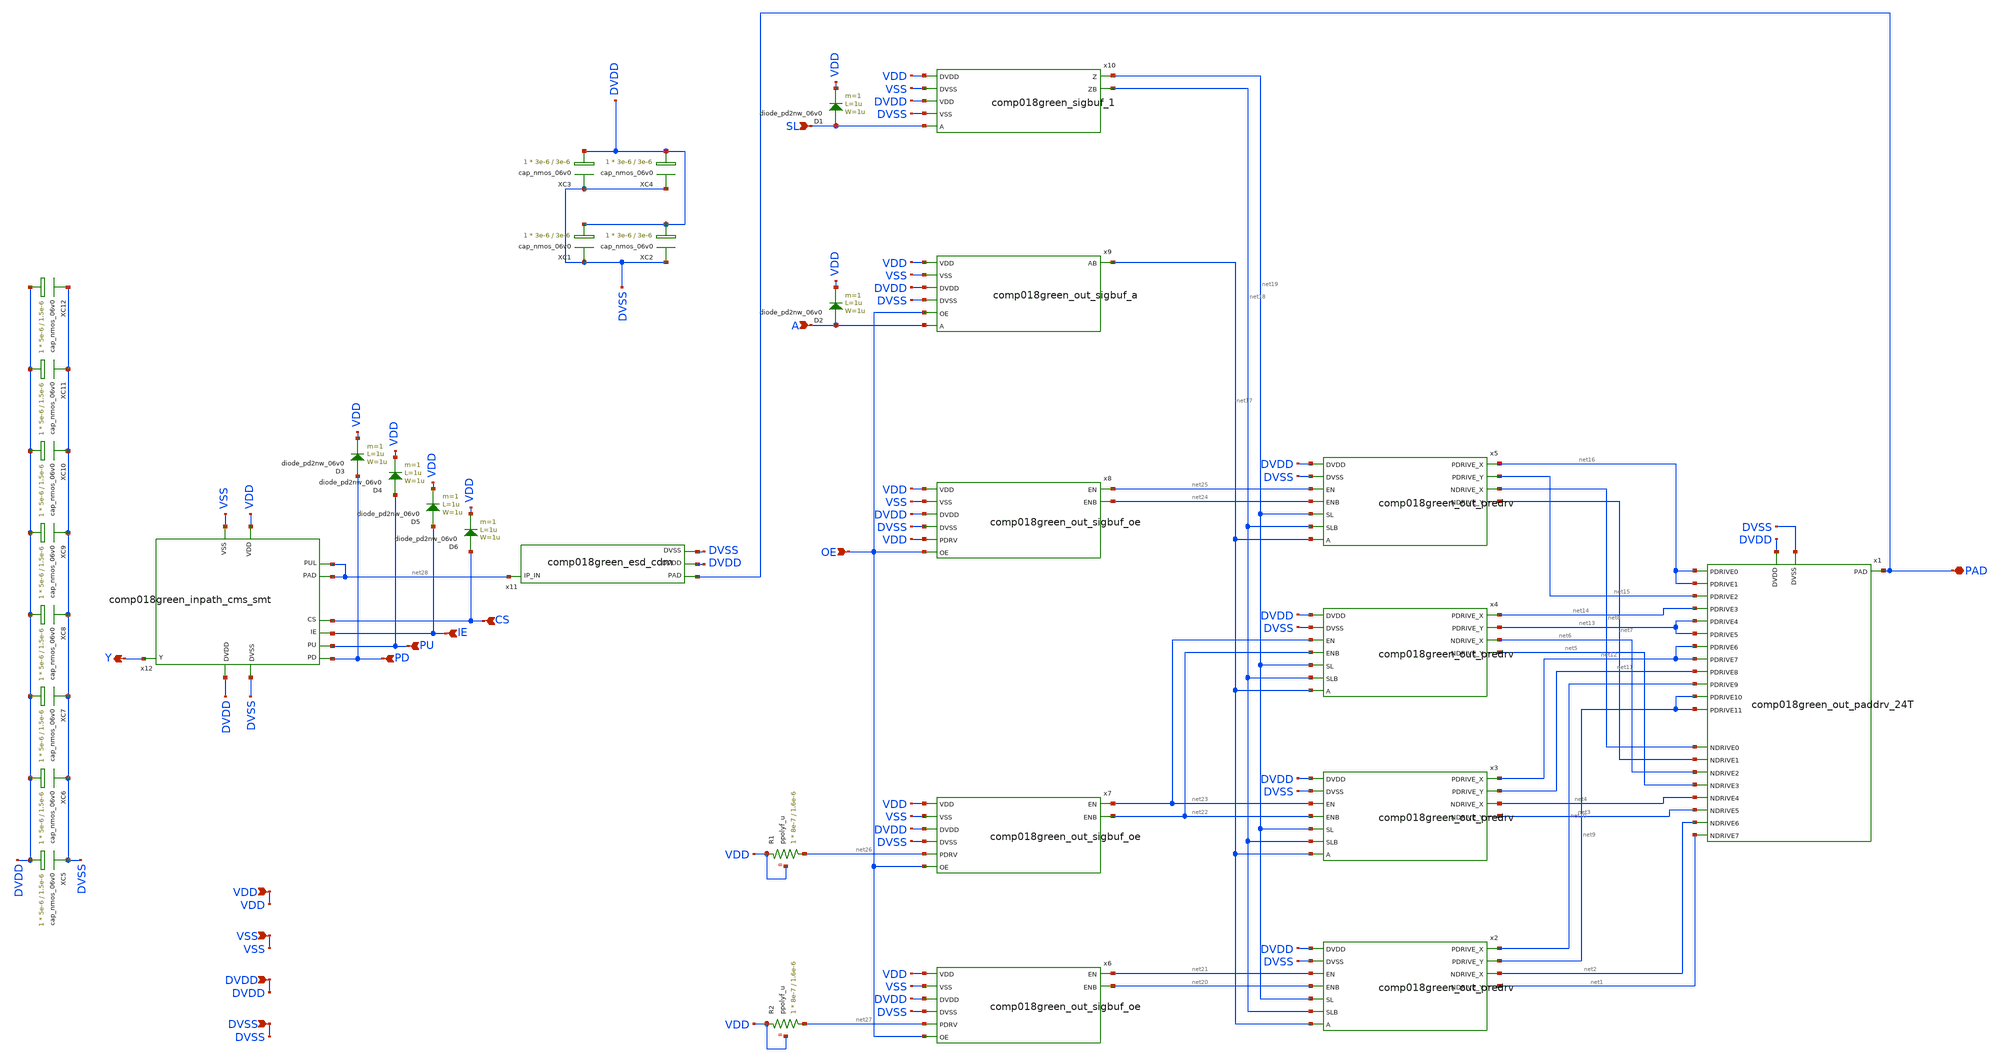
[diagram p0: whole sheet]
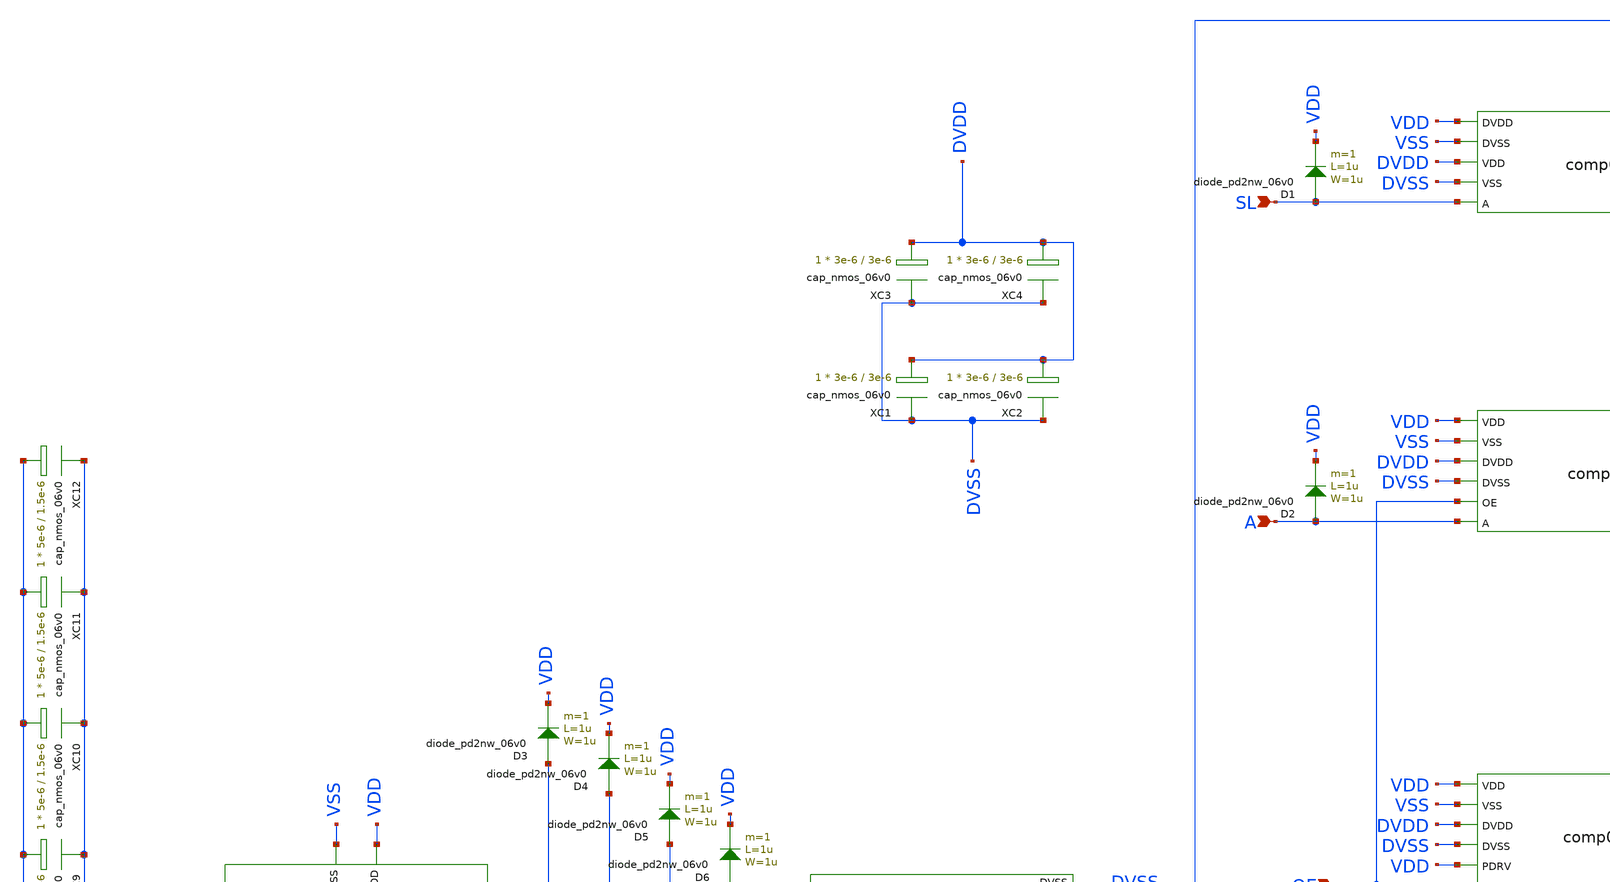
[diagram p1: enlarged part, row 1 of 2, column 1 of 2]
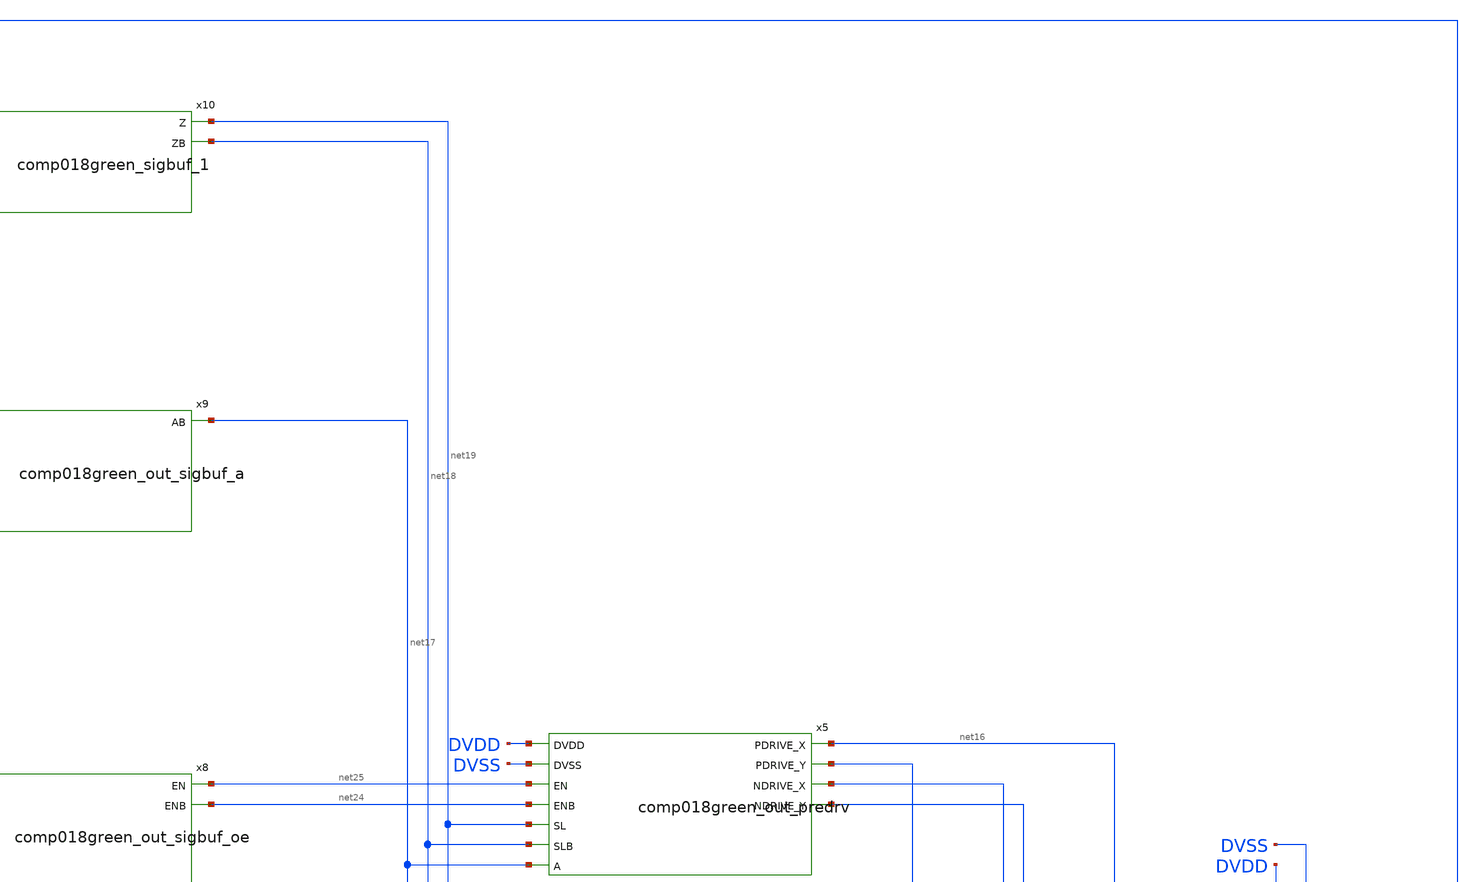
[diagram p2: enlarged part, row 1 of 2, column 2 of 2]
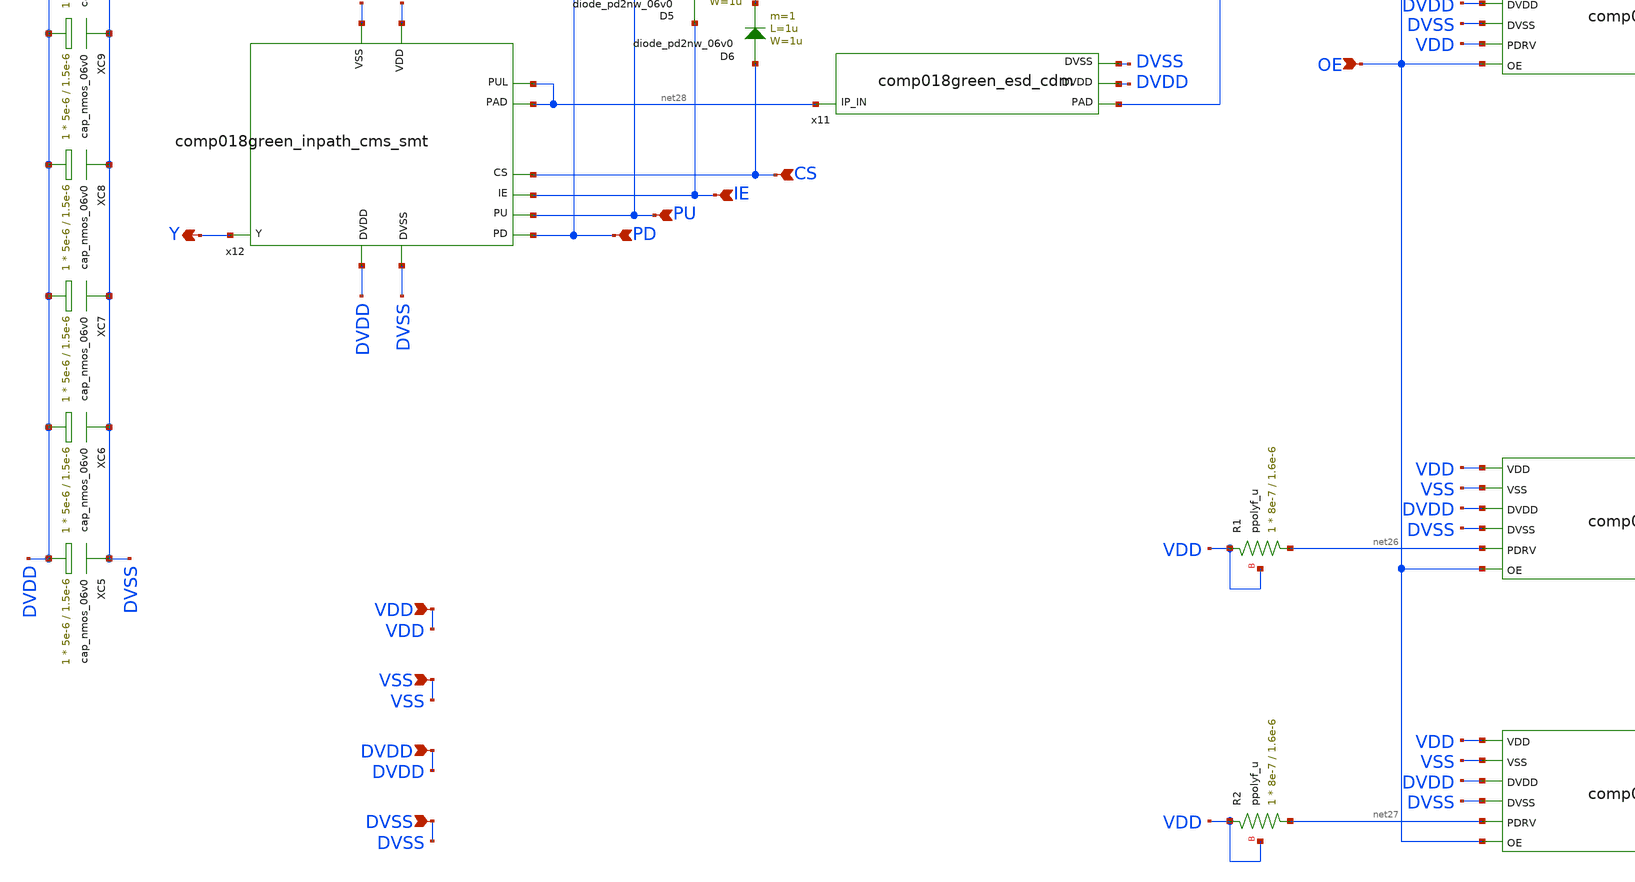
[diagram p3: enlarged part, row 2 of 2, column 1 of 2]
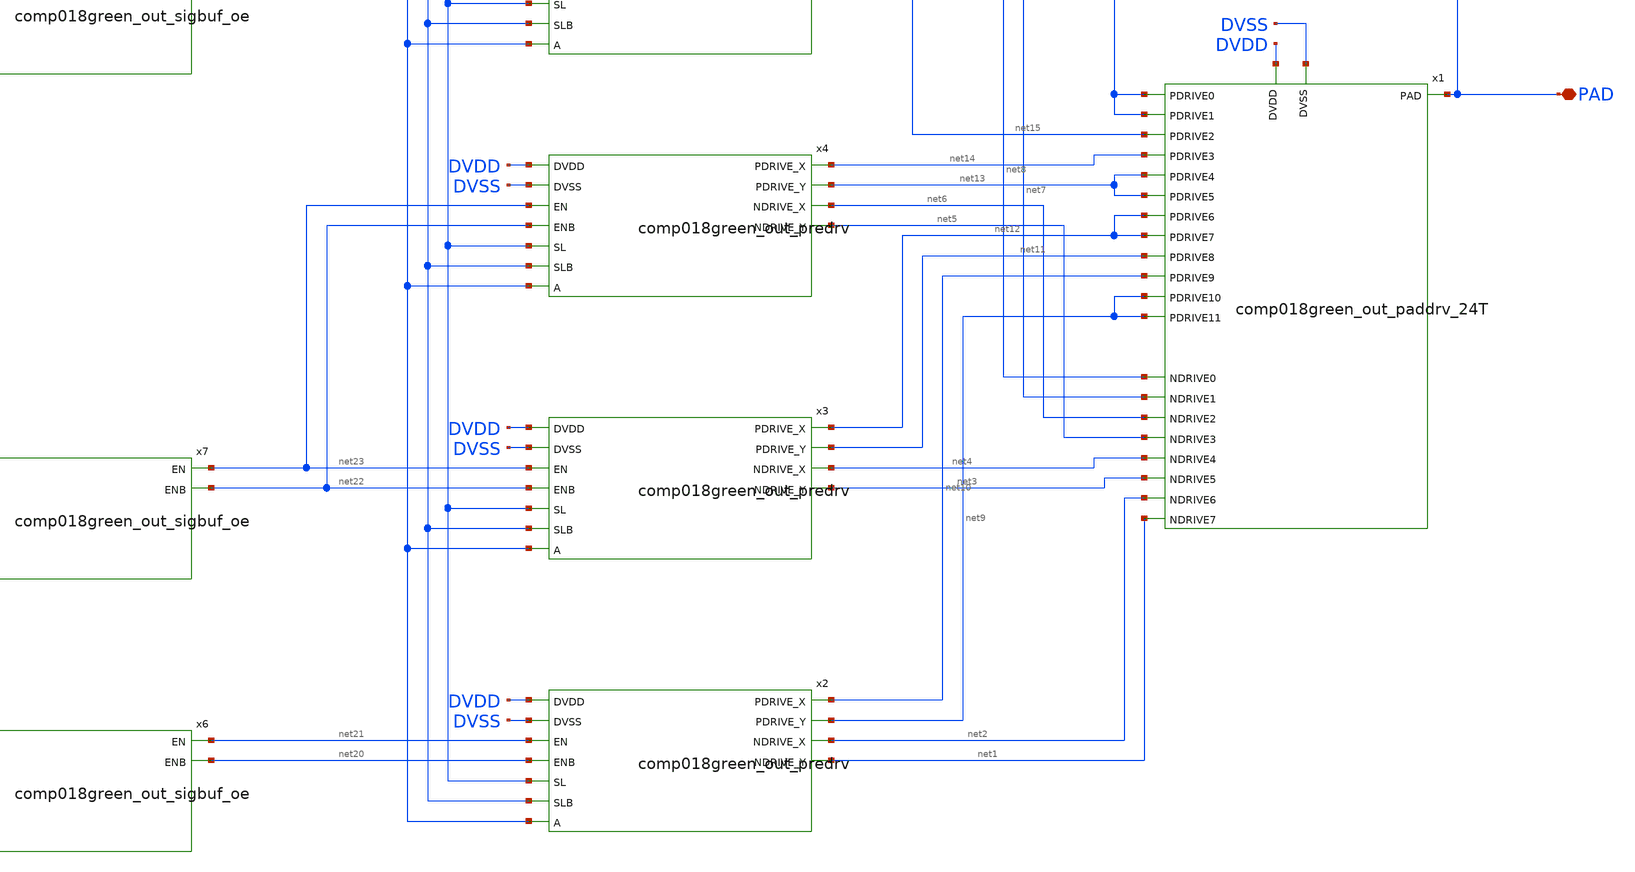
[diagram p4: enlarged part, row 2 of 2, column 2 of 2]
** sch_path: gf180mcu_fd_io__bi_24t/gf180mcu_fd_io__bi_24t.sch
**.subckt gf180mcu_fd_io__bi_24t SL A OE Y PAD PD PU IE CS VDD VSS DVDD DVSS
*.ipin SL
*.ipin A
*.ipin OE
*.opin Y
*.iopin PAD
*.ipin PD
*.ipin PU
*.ipin IE
*.ipin CS
*.ipin VDD
*.ipin VSS
*.ipin DVDD
*.ipin DVSS
x1 net12 net13 net14 net11 net15 net12 net16 net13 net10 net9 net9 net16 DVDD DVSS PAD net7 net1
+ net2 net3 net4 net5 net6 net8 comp018green_out_paddrv_24T
x2 DVDD net19 net10 net1 net9 net2 net20 net21 net17 net18 DVSS comp018green_out_predrv
x3 DVDD net19 net12 net3 net11 net4 net22 net23 net17 net18 DVSS comp018green_out_predrv
x4 DVDD net19 net14 net5 net13 net6 net22 net23 net17 net18 DVSS comp018green_out_predrv
x5 DVDD net19 net16 net7 net15 net8 net24 net25 net17 net18 DVSS comp018green_out_predrv
x6 VDD DVDD net21 net27 net20 OE DVSS VSS comp018green_out_sigbuf_oe
x7 VDD DVDD net23 net26 net22 OE DVSS VSS comp018green_out_sigbuf_oe
x8 VDD DVDD net25 VDD net24 OE DVSS VSS comp018green_out_sigbuf_oe
x9 VDD DVDD OE A net17 DVSS VSS comp018green_out_sigbuf_a
x10 VDD DVDD SL net19 net18 DVSS VSS comp018green_sigbuf_1
D1 SL VDD diode_pd2nw_06v0 area='1u * 1u ' pj='2*1u + 2*1u ' m=1
D2 A VDD diode_pd2nw_06v0 area='1u * 1u ' pj='2*1u + 2*1u ' m=1
XR1 net26 VDD VDD ppolyf_u r_width=8e-7 r_length=1.6e-6 m=1
XR2 net27 VDD VDD ppolyf_u r_width=8e-7 r_length=1.6e-6 m=1
x11 PAD net28 DVSS DVDD comp018green_esd_cdm
x12 PD PU net28 Y net28 IE CS DVDD VDD DVSS VSS comp018green_inpath_cms_smt
D3 PD VDD diode_pd2nw_06v0 area='1u * 1u ' pj='2*1u + 2*1u ' m=1
D4 PU VDD diode_pd2nw_06v0 area='1u * 1u ' pj='2*1u + 2*1u ' m=1
D5 IE VDD diode_pd2nw_06v0 area='1u * 1u ' pj='2*1u + 2*1u ' m=1
D6 CS VDD diode_pd2nw_06v0 area='1u * 1u ' pj='2*1u + 2*1u ' m=1
XC1 DVSS DVDD cap_nmos_06v0 c_width=3e-6 c_length=3e-6 m=1
XC2 DVSS DVDD cap_nmos_06v0 c_width=3e-6 c_length=3e-6 m=1
XC3 DVSS DVDD cap_nmos_06v0 c_width=3e-6 c_length=3e-6 m=1
XC4 DVSS DVDD cap_nmos_06v0 c_width=3e-6 c_length=3e-6 m=1
XC5 DVSS DVDD cap_nmos_06v0 c_width=5e-6 c_length=1.5e-6 m=1
XC6 DVSS DVDD cap_nmos_06v0 c_width=5e-6 c_length=1.5e-6 m=1
XC7 DVSS DVDD cap_nmos_06v0 c_width=5e-6 c_length=1.5e-6 m=1
XC8 DVSS DVDD cap_nmos_06v0 c_width=5e-6 c_length=1.5e-6 m=1
XC9 DVSS DVDD cap_nmos_06v0 c_width=5e-6 c_length=1.5e-6 m=1
XC10 DVSS DVDD cap_nmos_06v0 c_width=5e-6 c_length=1.5e-6 m=1
XC11 DVSS DVDD cap_nmos_06v0 c_width=5e-6 c_length=1.5e-6 m=1
XC12 DVSS DVDD cap_nmos_06v0 c_width=5e-6 c_length=1.5e-6 m=1
**.ends
.end
